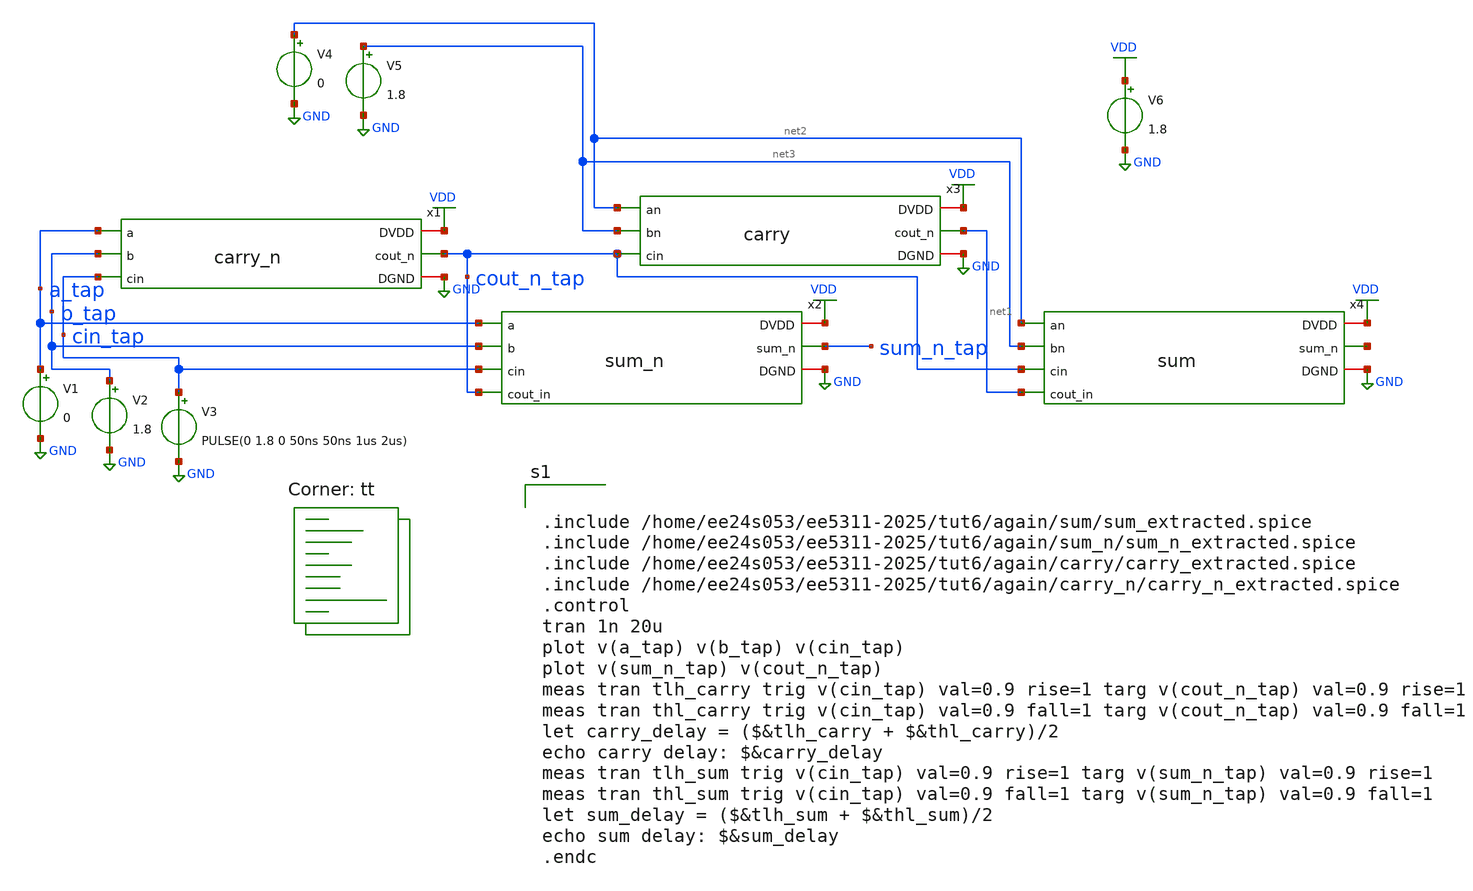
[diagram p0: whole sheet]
** sch_path: tut6/again/sim/adder_parasitics.sch
**.subckt adder_parasitics
x1 VDD a_tap b_tap cout_n_tap cin_tap GND carry_n
x2 VDD a_tap b_tap sum_n_tap cin_tap cout_n_tap GND sum_n
x3 VDD net2 net3 net1 cout_n_tap GND carry
x4 VDD net2 net4 net3 cout_n_tap net1 GND sum
V1 a_tap GND 0
V2 b_tap GND 1.8
V3 cin_tap GND PULSE(0 1.8 0 50ns 50ns 1us 2us)
V4 net2 GND 0
V5 net3 GND 1.8
V6 VDD GND 1.8
**** begin user architecture code


.include /home/ee24s053/ee5311-2025/tut6/again/sum/sum_extracted.spice
.include /home/ee24s053/ee5311-2025/tut6/again/sum_n/sum_n_extracted.spice
.include /home/ee24s053/ee5311-2025/tut6/again/carry/carry_extracted.spice
.include /home/ee24s053/ee5311-2025/tut6/again/carry_n/carry_n_extracted.spice
.control
tran 1n 20u
plot v(a_tap) v(b_tap) v(cin_tap)
plot v(sum_n_tap) v(cout_n_tap)
meas tran tlh_carry trig v(cin_tap) val=0.9 rise=1 targ v(cout_n_tap) val=0.9 rise=1
meas tran thl_carry trig v(cin_tap) val=0.9 fall=1 targ v(cout_n_tap) val=0.9 fall=1
let carry_delay = ($&tlh_carry + $&thl_carry)/2
echo carry delay: $&carry_delay
meas tran tlh_sum trig v(cin_tap) val=0.9 rise=1 targ v(sum_n_tap) val=0.9 rise=1
meas tran thl_sum trig v(cin_tap) val=0.9 fall=1 targ v(sum_n_tap) val=0.9 fall=1
let sum_delay = ($&tlh_sum + $&thl_sum)/2
echo sum delay: $&sum_delay
.endc

.lib $::SKYWATER_MODELS/sky130.lib.spice tt
**** end user architecture code
**.ends
.GLOBAL VDD
.GLOBAL GND
.end
